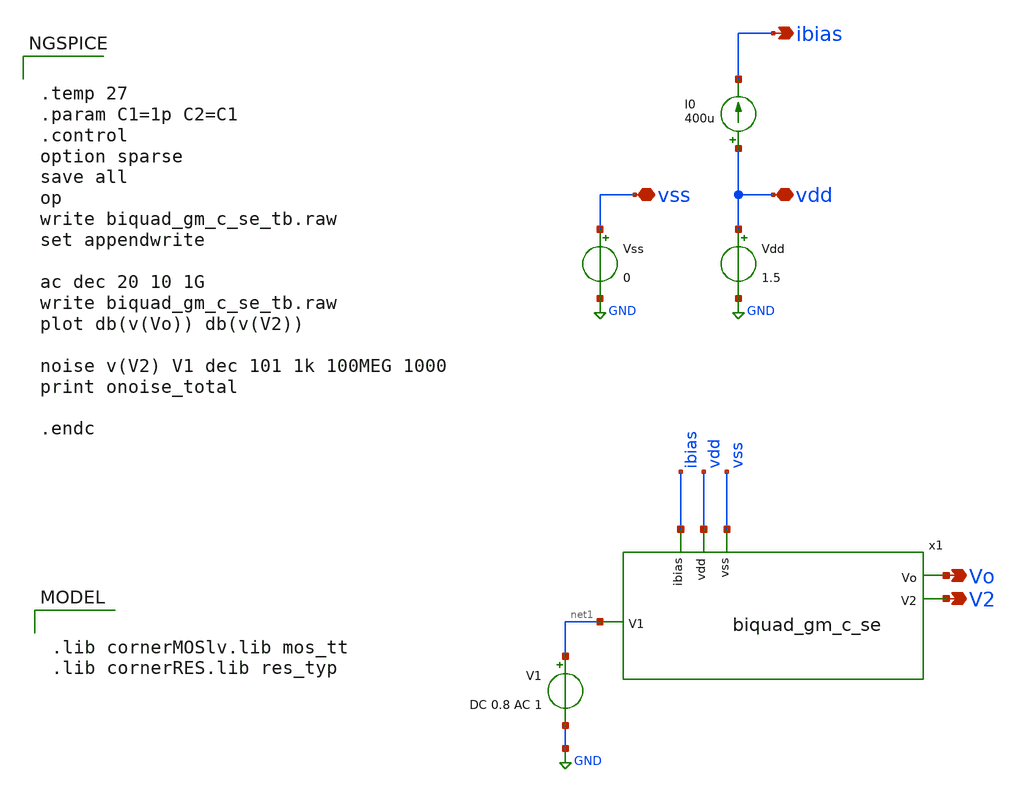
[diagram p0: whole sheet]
** sch_path: prj/template/3_Real_circuits/biquad_gm_c_se_tb.sch
* prj/template/3_Real_circuits/ota_gm_100u_se.sch:
* (c) 2024-2025 M. Meiners, Apache-2.0 license
**.subckt biquad_gm_c_se_tb vss vdd ibias Vo V2
*.iopin vss
*.iopin vdd
*.opin ibias
*.opin Vo
*.opin V2
V1 net1 GND DC 0.8 AC 1
Vss vss GND 0
Vdd vdd GND 1.5
I0 vdd ibias 400u
x1 Vo vdd ibias V2 vss net1 biquad_gm_c_se
**** begin user architecture code


.temp 27
.param C1=1p C2=C1
.control
option sparse
save all
op
write biquad_gm_c_se_tb.raw
set appendwrite

ac dec 20 10 1G
write biquad_gm_c_se_tb.raw
plot db(v(Vo)) db(v(V2))

noise v(V2) V1 dec 101 1k 100MEG 1000
print onoise_total

.endc



.lib cornerMOSlv.lib mos_tt
.lib cornerRES.lib res_typ

**** end user architecture code
**.ends

* expanding   symbol:  biquad_gm_c_se.sym # of pins=6
** sym_path: prj/template/3_Real_circuits/biquad_gm_c_se.sym
** sch_path: prj/template/3_Real_circuits/biquad_gm_c_se.sch
.subckt biquad_gm_c_se Vo vdd ibias V2 vss V1
*.ipin V1
*.opin Vo
*.opin V2
*.ipin ibias
*.iopin vdd
*.iopin vss
C1 vss V2 {C1} m=1
C2 vss Vo {C2} m=1
x1 vss V1 V2 ibias vdd vss ota_gm_100u_se
x2 vss V2 V2 ibias vdd vss ota_gm_100u_se
x3 vss V2 Vo ibias vdd vss ota_gm_100u_se
x4 vss Vo V2 ibias vdd vss ota_gm_100u_se
.ends


* expanding   symbol:  ota_gm_100u_se.sym # of pins=8
** sym_path: prj/template/3_Real_circuits/ota_gm_100u_se.sym
** sch_path: prj/template/3_Real_circuits/ota_gm_100u_se.sch
.subckt ota_gm_100u_se inp inn out ibias vdd vss
*.ipin ibias
*.iopin vdd
*.iopin vss
*.ipin inp
*.ipin inn
*.opin out
XM5 tail ibias vss vss sg13_lv_nmos w=14u l=5u ng=10 m=1 mm_ok=1
XM4 out gate_p vdd vdd sg13_lv_pmos w=31u l=5u ng=10 m=1 mm_ok=1
XM1 gate_p inp tail tail sg13_lv_nmos w=33u l=5u ng=10 m=1 mm_ok=1
XM2 out inn tail tail sg13_lv_nmos w=33u l=5u ng=10 m=1 mm_ok=1
XM3 gate_p gate_p vdd vdd sg13_lv_pmos w=31u l=5u ng=10 m=1 mm_ok=1
XM6 ibias ibias vss vss sg13_lv_nmos w=18u l=5u ng=10 m=1 mm_ok=1
.ends

.GLOBAL GND
.end
